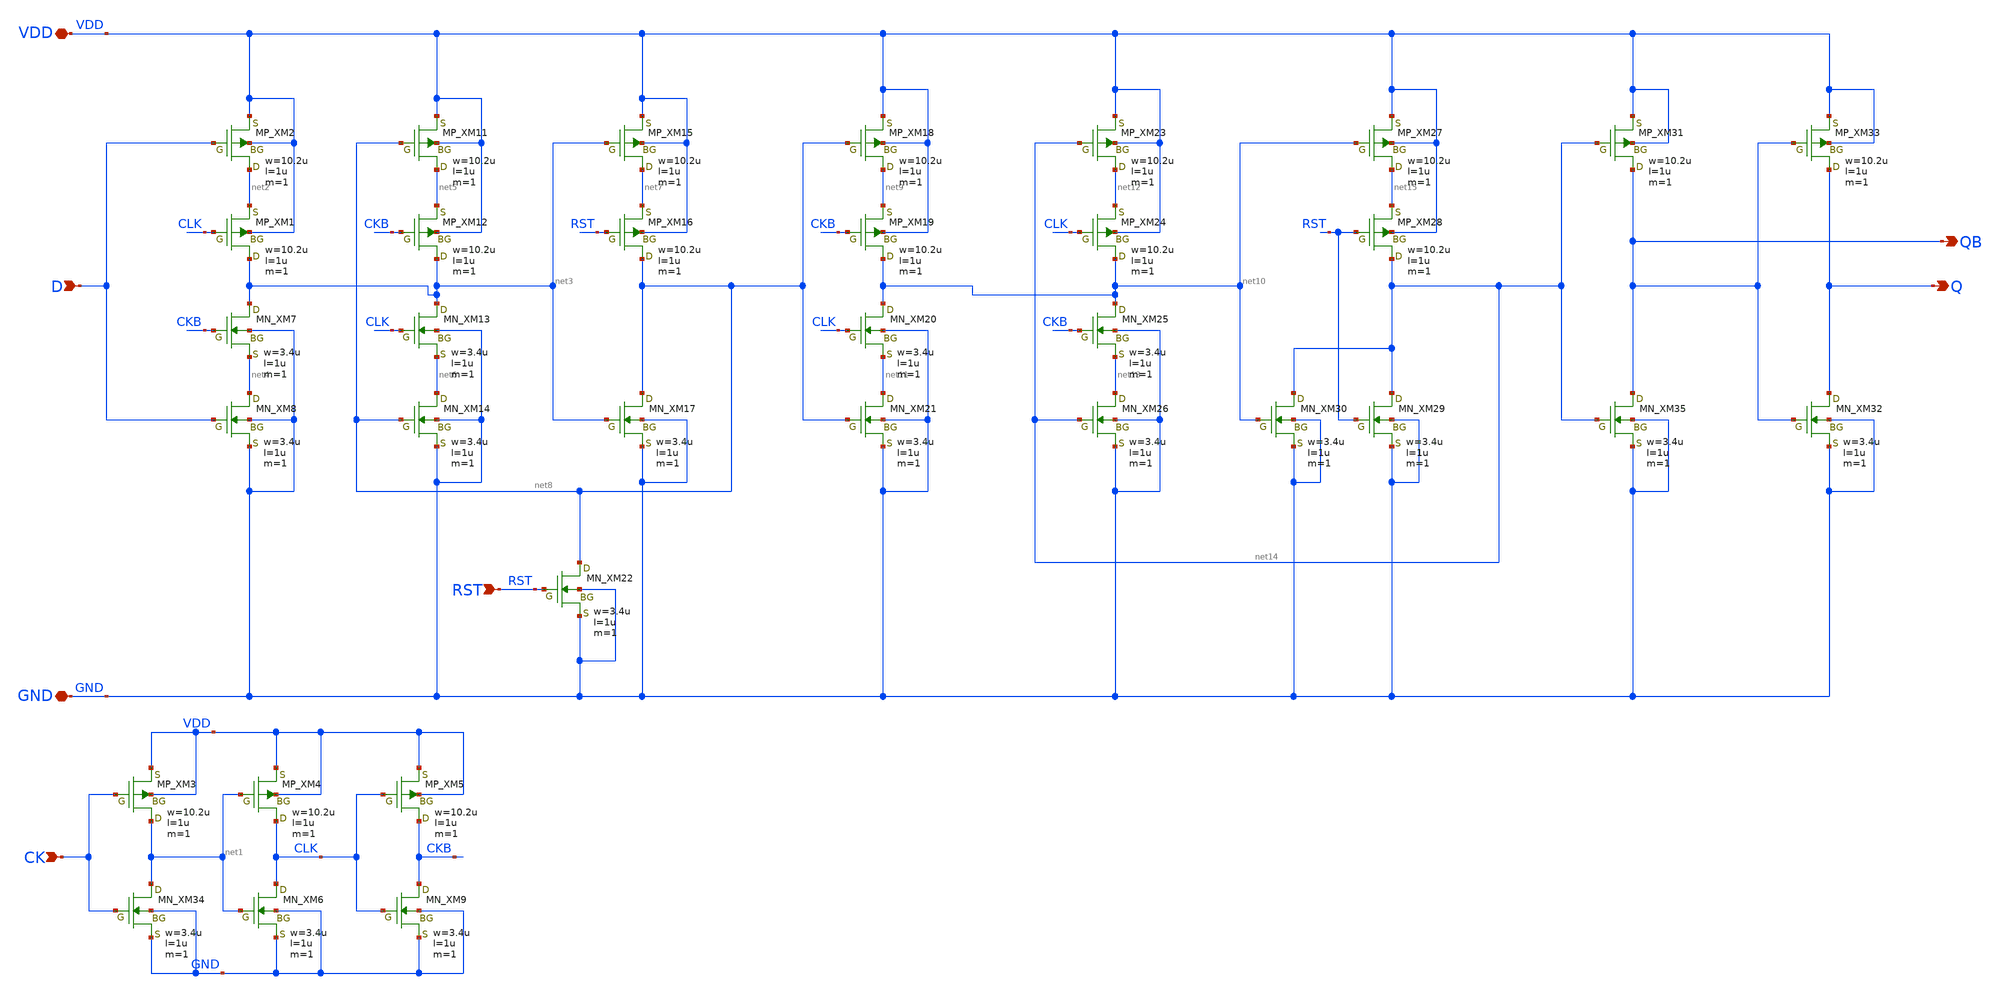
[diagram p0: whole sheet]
** sch_path: openIP62_rev1.0/IP62/Technology/tech/symbols/Xschem/IP62_5_stdcell/DFFR.sch
**.subckt DFFR VDD GND CK D Q QB RST
*.iopin VDD
*.iopin GND
*.ipin CK
*.ipin D
*.opin Q
*.opin QB
*.ipin RST
XM2 net2 D VDD VDD PMOS w=10.2u l=1u as=0 ad=0 ps=0 pd=0 nrd=0 nrs=0 m=1
XM1 net3 CLK net2 VDD PMOS w=10.2u l=1u as=0 ad=0 ps=0 pd=0 nrd=0 nrs=0 m=1
XM11 net5 net8 VDD VDD PMOS w=10.2u l=1u as=0 ad=0 ps=0 pd=0 nrd=0 nrs=0 m=1
XM12 net3 CKB net5 VDD PMOS w=10.2u l=1u as=0 ad=0 ps=0 pd=0 nrd=0 nrs=0 m=1
XM15 net7 net3 VDD VDD PMOS w=10.2u l=1u as=0 ad=0 ps=0 pd=0 nrd=0 nrs=0 m=1
XM16 net8 RST net7 VDD PMOS w=10.2u l=1u as=0 ad=0 ps=0 pd=0 nrd=0 nrs=0 m=1
XM18 net9 net8 VDD VDD PMOS w=10.2u l=1u as=0 ad=0 ps=0 pd=0 nrd=0 nrs=0 m=1
XM19 net10 CKB net9 VDD PMOS w=10.2u l=1u as=0 ad=0 ps=0 pd=0 nrd=0 nrs=0 m=1
XM23 net12 net14 VDD VDD PMOS w=10.2u l=1u as=0 ad=0 ps=0 pd=0 nrd=0 nrs=0 m=1
XM24 net10 CLK net12 VDD PMOS w=10.2u l=1u as=0 ad=0 ps=0 pd=0 nrd=0 nrs=0 m=1
XM27 net15 net10 VDD VDD PMOS w=10.2u l=1u as=0 ad=0 ps=0 pd=0 nrd=0 nrs=0 m=1
XM28 net14 RST net15 VDD PMOS w=10.2u l=1u as=0 ad=0 ps=0 pd=0 nrd=0 nrs=0 m=1
XM31 QB net14 VDD VDD PMOS w=10.2u l=1u as=0 ad=0 ps=0 pd=0 nrd=0 nrs=0 m=1
XM33 Q QB VDD VDD PMOS w=10.2u l=1u as=0 ad=0 ps=0 pd=0 nrd=0 nrs=0 m=1
XM35 QB net14 GND GND NMOS w=3.4u l=1u as=0 ad=0 ps=0 pd=0 nrd=0 nrs=0 m=1
XM32 Q QB GND GND NMOS w=3.4u l=1u as=0 ad=0 ps=0 pd=0 nrd=0 nrs=0 m=1
XM29 net14 RST GND GND NMOS w=3.4u l=1u as=0 ad=0 ps=0 pd=0 nrd=0 nrs=0 m=1
XM30 net14 net10 GND GND NMOS w=3.4u l=1u as=0 ad=0 ps=0 pd=0 nrd=0 nrs=0 m=1
XM25 net10 CKB net13 GND NMOS w=3.4u l=1u as=0 ad=0 ps=0 pd=0 nrd=0 nrs=0 m=1
XM26 net13 net14 GND GND NMOS w=3.4u l=1u as=0 ad=0 ps=0 pd=0 nrd=0 nrs=0 m=1
XM20 net10 CLK net11 GND NMOS w=3.4u l=1u as=0 ad=0 ps=0 pd=0 nrd=0 nrs=0 m=1
XM21 net11 net8 GND GND NMOS w=3.4u l=1u as=0 ad=0 ps=0 pd=0 nrd=0 nrs=0 m=1
XM17 net8 net3 GND GND NMOS w=3.4u l=1u as=0 ad=0 ps=0 pd=0 nrd=0 nrs=0 m=1
XM22 net8 RST GND GND NMOS w=3.4u l=1u as=0 ad=0 ps=0 pd=0 nrd=0 nrs=0 m=1
XM13 net3 CLK net6 GND NMOS w=3.4u l=1u as=0 ad=0 ps=0 pd=0 nrd=0 nrs=0 m=1
XM14 net6 net8 GND GND NMOS w=3.4u l=1u as=0 ad=0 ps=0 pd=0 nrd=0 nrs=0 m=1
XM7 net3 CKB net4 GND NMOS w=3.4u l=1u as=0 ad=0 ps=0 pd=0 nrd=0 nrs=0 m=1
XM8 net4 D GND GND NMOS w=3.4u l=1u as=0 ad=0 ps=0 pd=0 nrd=0 nrs=0 m=1
XM3 net1 CK VDD VDD PMOS w=10.2u l=1u as=0 ad=0 ps=0 pd=0 nrd=0 nrs=0 m=1
XM4 CLK net1 VDD VDD PMOS w=10.2u l=1u as=0 ad=0 ps=0 pd=0 nrd=0 nrs=0 m=1
XM5 CKB CLK VDD VDD PMOS w=10.2u l=1u as=0 ad=0 ps=0 pd=0 nrd=0 nrs=0 m=1
XM34 net1 CK GND GND NMOS w=3.4u l=1u as=0 ad=0 ps=0 pd=0 nrd=0 nrs=0 m=1
XM6 CLK net1 GND GND NMOS w=3.4u l=1u as=0 ad=0 ps=0 pd=0 nrd=0 nrs=0 m=1
XM9 CKB CLK GND GND NMOS w=3.4u l=1u as=0 ad=0 ps=0 pd=0 nrd=0 nrs=0 m=1
**.ends
.end
